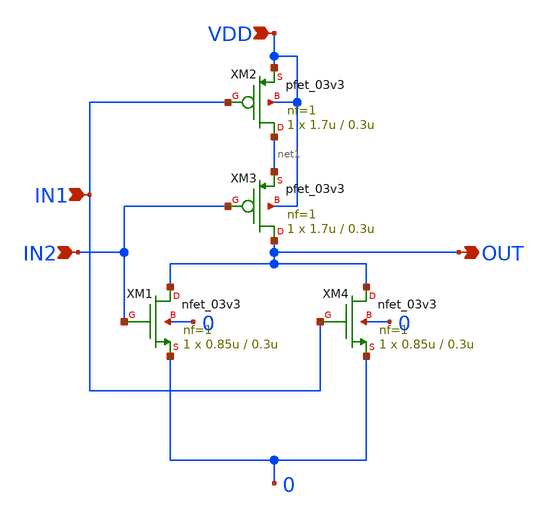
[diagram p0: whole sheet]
** sch_path: initial_notebooks_2023/accepted_notebooks/Current-Steering-DAC/DAC/NOR2_1.sch
**.subckt NOR2_1 VDD IN1 IN2 OUT
*.ipin VDD
*.ipin IN1
*.ipin IN2
*.opin OUT
XM1 OUT IN2 0 0 nfet_03v3 L=0.3u W=0.85u nf=1 ad='int((nf+1)/2) * W/nf * 0.18u' as='int((nf+2)/2) * W/nf * 0.18u'
+ pd='2*int((nf+1)/2) * (W/nf + 0.18u)' ps='2*int((nf+2)/2) * (W/nf + 0.18u)' nrd='0.18u / W' nrs='0.18u / W'
+ sa=0 sb=0 sd=0 m=1
XM2 net1 IN1 VDD VDD pfet_03v3 L=0.3u W=1.7u nf=1 ad='int((nf+1)/2) * W/nf * 0.18u' as='int((nf+2)/2) * W/nf * 0.18u'
+ pd='2*int((nf+1)/2) * (W/nf + 0.18u)' ps='2*int((nf+2)/2) * (W/nf + 0.18u)' nrd='0.18u / W' nrs='0.18u / W'
+ sa=0 sb=0 sd=0 m=1
XM3 OUT IN2 net1 VDD pfet_03v3 L=0.3u W=1.7u nf=1 ad='int((nf+1)/2) * W/nf * 0.18u' as='int((nf+2)/2) * W/nf * 0.18u'
+ pd='2*int((nf+1)/2) * (W/nf + 0.18u)' ps='2*int((nf+2)/2) * (W/nf + 0.18u)' nrd='0.18u / W' nrs='0.18u / W'
+ sa=0 sb=0 sd=0 m=1
XM4 OUT IN1 0 0 nfet_03v3 L=0.3u W=0.85u nf=1 ad='int((nf+1)/2) * W/nf * 0.18u' as='int((nf+2)/2) * W/nf * 0.18u'
+ pd='2*int((nf+1)/2) * (W/nf + 0.18u)' ps='2*int((nf+2)/2) * (W/nf + 0.18u)' nrd='0.18u / W' nrs='0.18u / W'
+ sa=0 sb=0 sd=0 m=1
**.ends
.end
